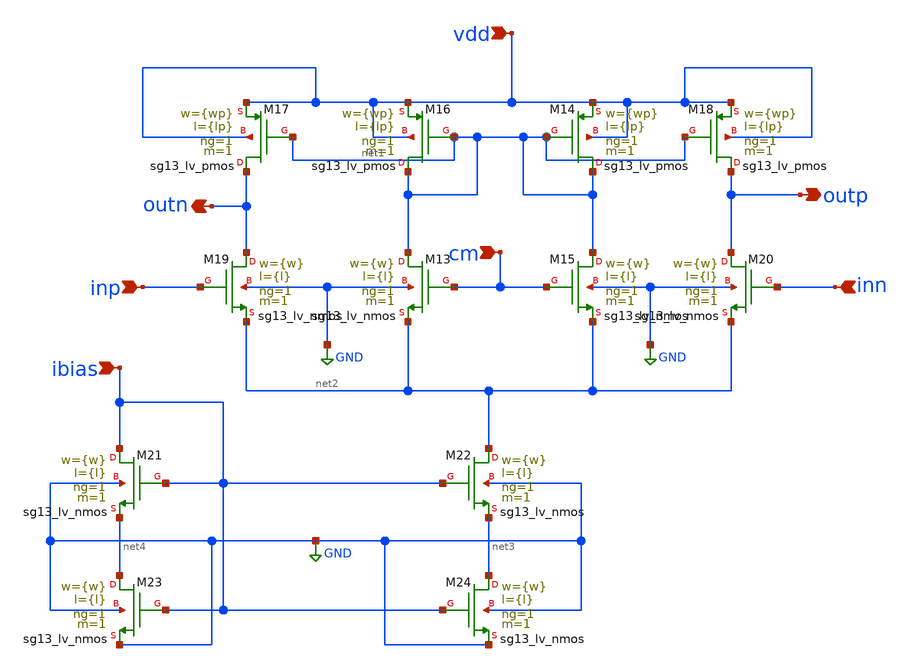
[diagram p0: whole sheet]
** sch_path: 2_Ideal_Cir/ota_gm_100u.sch
**.subckt ota_gm_100u inp vdd inn outp cm ibias outn
*.ipin inp
*.ipin vdd
*.ipin inn
*.opin outp
*.ipin cm
*.ipin ibias
*.opin outn
XM13 net1 cm net2 GND sg13_lv_nmos w={w} l={l} ng=1 m=1 mm_ok=1
XM14 net1 net1 vdd vdd sg13_lv_pmos w={wp} l={lp} ng=1 m=1 mm_ok=1
XM15 net1 cm net2 GND sg13_lv_nmos w={w} l={l} ng=1 m=1 mm_ok=1
XM16 net1 net1 vdd vdd sg13_lv_pmos w={wp} l={lp} ng=1 m=1 mm_ok=1
XM17 outn net1 vdd vdd sg13_lv_pmos w={wp} l={lp} ng=1 m=1 mm_ok=1
XM18 outp net1 vdd vdd sg13_lv_pmos w={wp} l={lp} ng=1 m=1 mm_ok=1
XM19 outn inp net2 GND sg13_lv_nmos w={w} l={l} ng=1 m=1 mm_ok=1
XM20 outp inn net2 GND sg13_lv_nmos w={w} l={l} ng=1 m=1 mm_ok=1
XM21 ibias ibias net4 GND sg13_lv_nmos w={w} l={l} ng=1 m=1 mm_ok=1
XM22 net2 ibias net3 GND sg13_lv_nmos w={w} l={l} ng=1 m=1 mm_ok=1
XM23 net4 ibias GND GND sg13_lv_nmos w={w} l={l} ng=1 m=1 mm_ok=1
XM24 net3 ibias GND GND sg13_lv_nmos w={w} l={l} ng=1 m=1 mm_ok=1
**.ends
.GLOBAL GND
.end
